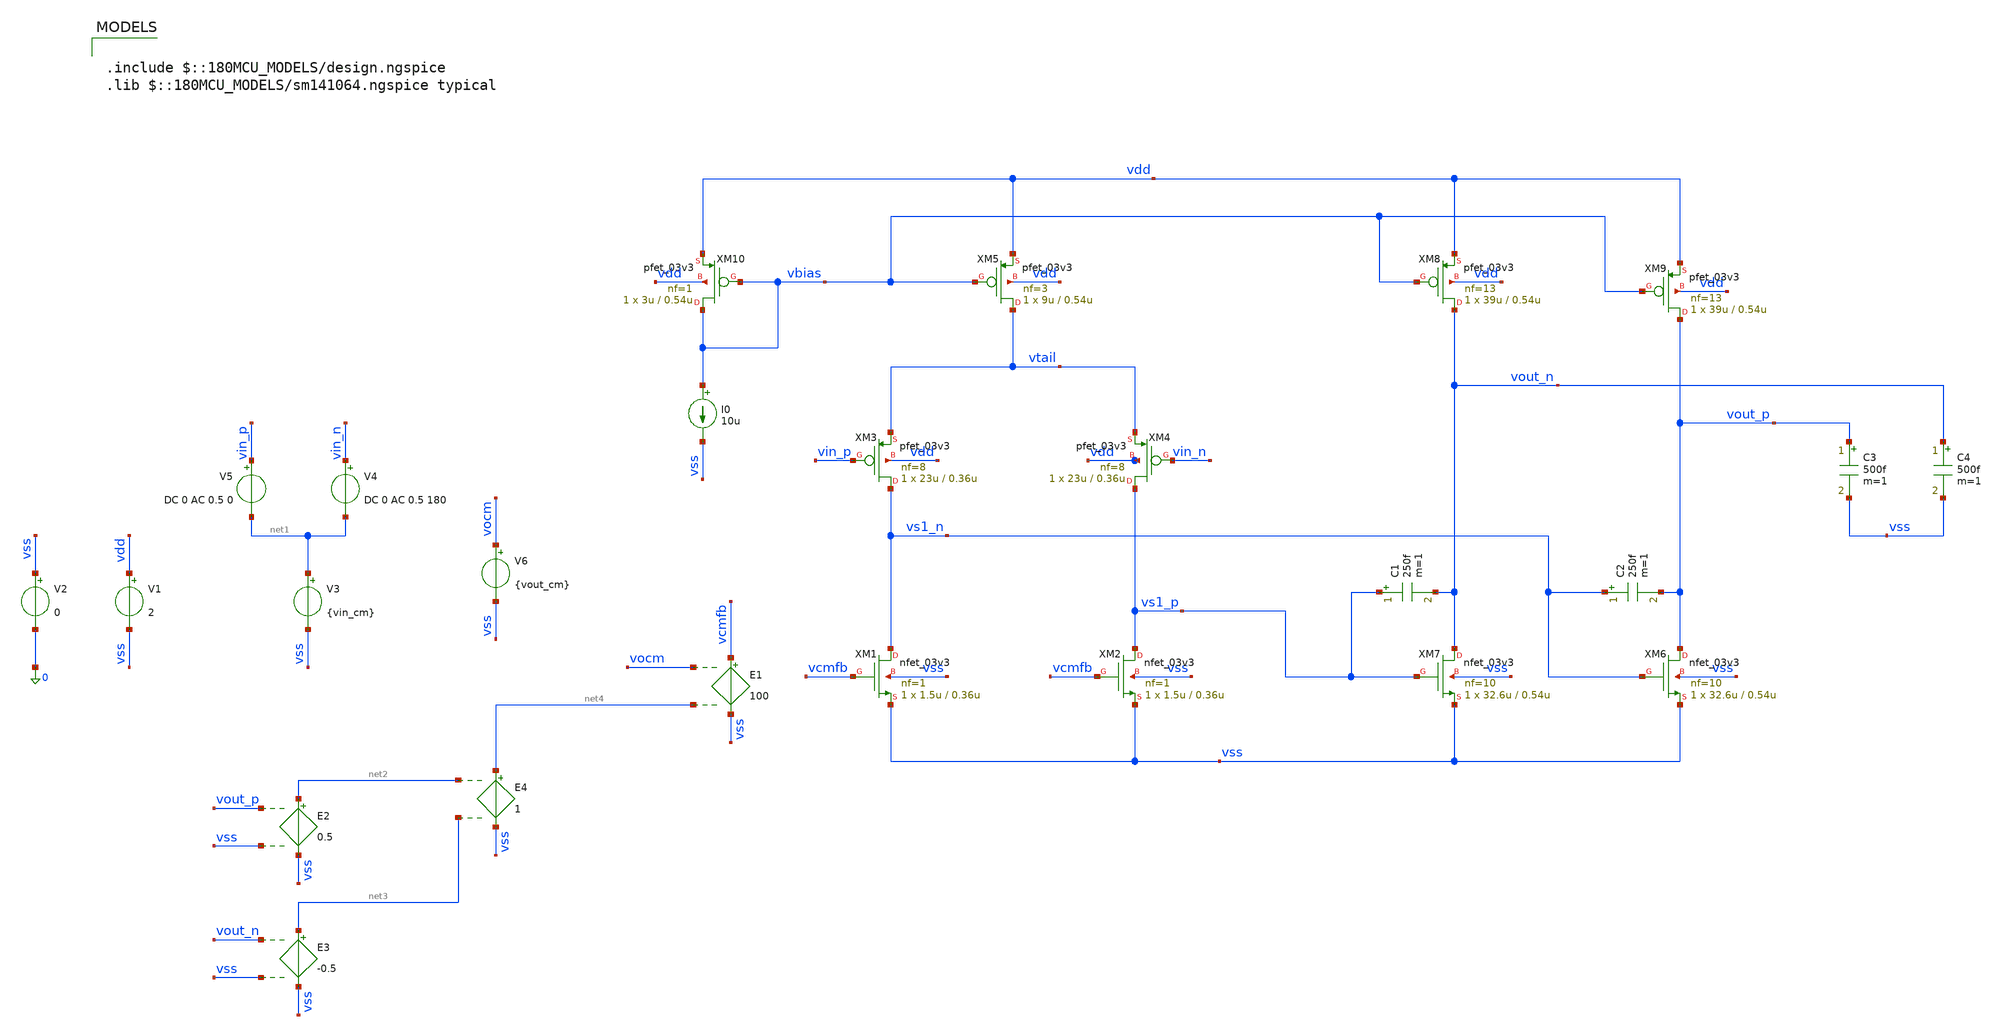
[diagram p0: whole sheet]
** sch_path: xschem/prototype_amp/prototype_amp.sch
**.subckt prototype_amp
XM1 vs1_n vcmfb vss vss nfet_03v3 L=0.36u W=1.5u nf=1 ad='int((nf+1)/2) * W/nf * 0.18u' as='int((nf+2)/2) * W/nf * 0.18u'
+ pd='2*int((nf+1)/2) * (W/nf + 0.18u)' ps='2*int((nf+2)/2) * (W/nf + 0.18u)' nrd='0.18u / W' nrs='0.18u / W'
+ sa=0 sb=0 sd=0 m=1
XM3 vs1_n vin_p vtail vdd pfet_03v3 L=0.36u W=23u nf=8 ad='int((nf+1)/2) * W/nf * 0.18u' as='int((nf+2)/2) * W/nf * 0.18u'
+ pd='2*int((nf+1)/2) * (W/nf + 0.18u)' ps='2*int((nf+2)/2) * (W/nf + 0.18u)' nrd='0.18u / W' nrs='0.18u / W'
+ sa=0 sb=0 sd=0 m=1
XM5 vtail vbias vdd vdd pfet_03v3 L=0.54u W=9u nf=3 ad='int((nf+1)/2) * W/nf * 0.18u' as='int((nf+2)/2) * W/nf * 0.18u'
+ pd='2*int((nf+1)/2) * (W/nf + 0.18u)' ps='2*int((nf+2)/2) * (W/nf + 0.18u)' nrd='0.18u / W' nrs='0.18u / W'
+ sa=0 sb=0 sd=0 m=1
XM7 vout_n vs1_p vss vss nfet_03v3 L=0.54u W=32.6u nf=10 ad='int((nf+1)/2) * W/nf * 0.18u' as='int((nf+2)/2) * W/nf * 0.18u'
+ pd='2*int((nf+1)/2) * (W/nf + 0.18u)' ps='2*int((nf+2)/2) * (W/nf + 0.18u)' nrd='0.18u / W' nrs='0.18u / W'
+ sa=0 sb=0 sd=0 m=1
C1 vs1_p vout_n 250f m=1
C2 vs1_n vout_p 250f m=1
C3 vout_p vss 500f m=1
C4 vout_n vss 500f m=1
XM8 vout_n vbias vdd vdd pfet_03v3 L=0.54u W=39u nf=13 ad='int((nf+1)/2) * W/nf * 0.18u' as='int((nf+2)/2) * W/nf * 0.18u'
+ pd='2*int((nf+1)/2) * (W/nf + 0.18u)' ps='2*int((nf+2)/2) * (W/nf + 0.18u)' nrd='0.18u / W' nrs='0.18u / W'
+ sa=0 sb=0 sd=0 m=1
XM10 vbias vbias vdd vdd pfet_03v3 L=0.54u W=3u nf=1 ad='int((nf+1)/2) * W/nf * 0.18u' as='int((nf+2)/2) * W/nf * 0.18u'
+ pd='2*int((nf+1)/2) * (W/nf + 0.18u)' ps='2*int((nf+2)/2) * (W/nf + 0.18u)' nrd='0.18u / W' nrs='0.18u / W'
+ sa=0 sb=0 sd=0 m=1
I0 vbias vss 10u
XM9 vout_p vbias vdd vdd pfet_03v3 L=0.54u W=39u nf=13 ad='int((nf+1)/2) * W/nf * 0.18u' as='int((nf+2)/2) * W/nf * 0.18u'
+ pd='2*int((nf+1)/2) * (W/nf + 0.18u)' ps='2*int((nf+2)/2) * (W/nf + 0.18u)' nrd='0.18u / W' nrs='0.18u / W'
+ sa=0 sb=0 sd=0 m=1
V1 vdd vss 2
V2 vss 0 0
V3 net1 vss {vin_cm}
V5 vin_p net1 DC 0 AC 0.5 0
V4 vin_n net1 DC 0 AC 0.5 180
E1 vcmfb vss vocm net4 100
E2 net2 vss vout_p vss 0.5
E3 net3 vss vout_n vss -0.5
E4 net4 vss net2 net3 1
V6 vocm vss {vout_cm}
XM4 vs1_p vin_n vtail vdd pfet_03v3 L=0.36u W=23u nf=8 ad='int((nf+1)/2) * W/nf * 0.18u' as='int((nf+2)/2) * W/nf * 0.18u'
+ pd='2*int((nf+1)/2) * (W/nf + 0.18u)' ps='2*int((nf+2)/2) * (W/nf + 0.18u)' nrd='0.18u / W' nrs='0.18u / W'
+ sa=0 sb=0 sd=0 m=1
XM2 vs1_p vcmfb vss vss nfet_03v3 L=0.36u W=1.5u nf=1 ad='int((nf+1)/2) * W/nf * 0.18u' as='int((nf+2)/2) * W/nf * 0.18u'
+ pd='2*int((nf+1)/2) * (W/nf + 0.18u)' ps='2*int((nf+2)/2) * (W/nf + 0.18u)' nrd='0.18u / W' nrs='0.18u / W'
+ sa=0 sb=0 sd=0 m=1
XM6 vout_p vs1_n vss vss nfet_03v3 L=0.54u W=32.6u nf=10 ad='int((nf+1)/2) * W/nf * 0.18u' as='int((nf+2)/2) * W/nf * 0.18u'
+ pd='2*int((nf+1)/2) * (W/nf + 0.18u)' ps='2*int((nf+2)/2) * (W/nf + 0.18u)' nrd='0.18u / W' nrs='0.18u / W'
+ sa=0 sb=0 sd=0 m=1
**** begin user architecture code

.param vin_cm=0.8
.param vout_cm=1
.control
save all
save @m.xm1.m0[id] @m.xm1.m0[gm] @m.xm1.m0[gds]
save @m.xm3.m0[id] @m.xm3.m0[gm] @m.xm3.m0[gds]
save @m.xm6.m0[id] @m.xm6.m0[gm] @m.xm6.m0[gds]
save @m.xm8.m0[id] @m.xm8.m0[gm] @m.xm8.m0[gds]

op
ac dec 10 1 1G

setplot ac1
let vdiff = v(vout_p) - v(vout_n)
write output.raw
.endc


.include $::180MCU_MODELS/design.ngspice
.lib $::180MCU_MODELS/sm141064.ngspice typical

**** end user architecture code
**.ends
.end
